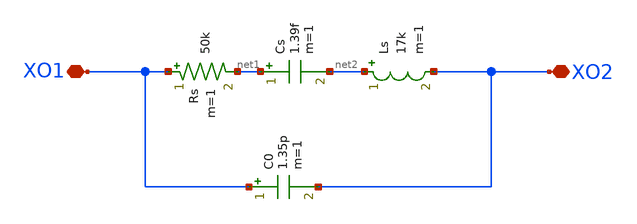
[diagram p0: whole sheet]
** sch_path: xtal_model.sch
**.subckt xtal_model XO2 XO1
*.iopin XO2
*.iopin XO1
Rs XO1 net1 50k m=1
Cs net1 net2 1.39f m=1
C0 XO1 XO2 1.35p m=1
Ls net2 XO2 17k m=1
**.ends
.end
